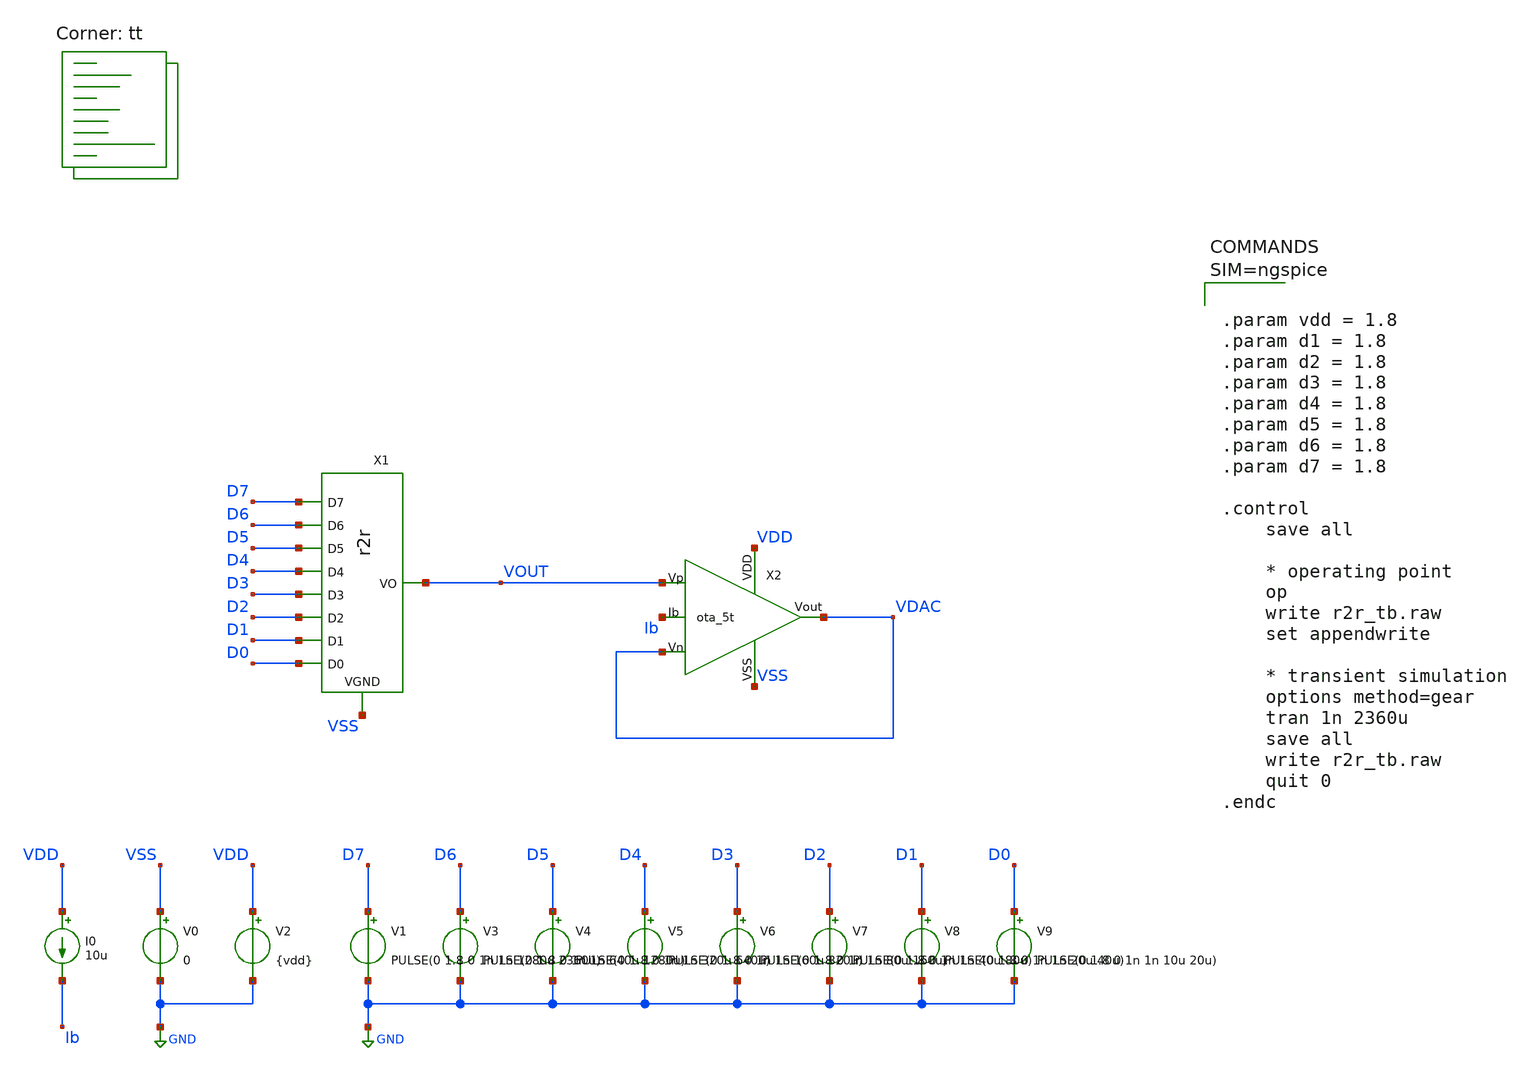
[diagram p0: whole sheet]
** sch_path: xschem/dac_tb.sch
**.subckt dac_tb
X1 D7 D6 D5 D4 D3 D2 D1 D0 VOUT VSS r2r
V0 VSS GND 0
V2 VDD GND {vdd}
V9 D0 GND PULSE(0 1.8 0 1n 1n 10u 20u)
V8 D1 GND PULSE(0 1.8 0 1n 1n 20u 40u)
V7 D2 GND PULSE(0 1.8 0 1n 1n 40u 80u)
V6 D3 GND PULSE(0 1.8 0 1n 1n 80u 160u)
V5 D4 GND PULSE(0 1.8 0 1n 1n 160u 320u)
V4 D5 GND PULSE(0 1.8 0 1n 1n 320u 640u)
V3 D6 GND PULSE(0 1.8 0 1n 1n 640u 1280u)
V1 D7 GND PULSE(0 1.8 0 1n 1n 1280u 2360u)
X2 Ib VDAC VOUT VDAC VDD VSS ota_5t
I0 VDD Ib 10u
**** begin user architecture code



.param vdd = 1.8
.param d1 = 1.8
.param d2 = 1.8
.param d3 = 1.8
.param d4 = 1.8
.param d5 = 1.8
.param d6 = 1.8
.param d7 = 1.8

.control
    save all

    * operating point
    op
    write r2r_tb.raw
    set appendwrite

    * transient simulation
    options method=gear
    tran 1n 2360u
    save all
    write r2r_tb.raw
    quit 0
.endc



.lib $::SKYWATER_MODELS/sky130.lib.spice tt
**** end user architecture code
**.ends

* expanding   symbol:  analog/projects/sky130/r2r-dac/xschem/r2r.sym # of pins=10
** sym_path: xschem/r2r.sym
** sch_path: xschem/r2r.sch
.subckt r2r D7 D6 D5 D4 D3 D2 D1 D0 VO VGND
*.ipin D0
*.ipin D1
*.ipin D2
*.ipin D3
*.ipin D4
*.ipin D5
*.ipin D6
*.ipin D7
*.opin VO
*.iopin VGND
XR8 net1 VGND VGND sky130_fd_pr__res_high_po_1p41 L=50 mult=1 m=1
XR1 net2 net1 VGND sky130_fd_pr__res_high_po_1p41 L=50 mult=1 m=1
XR2 net3 D0 VGND sky130_fd_pr__res_high_po_1p41 L=50 mult=1 m=1
XR3 net2 net3 VGND sky130_fd_pr__res_high_po_1p41 L=50 mult=1 m=1
XR4 net2 net5 VGND sky130_fd_pr__res_high_po_1p41 L=50 mult=1 m=1
XR5 net4 D1 VGND sky130_fd_pr__res_high_po_1p41 L=50 mult=1 m=1
XR6 net5 net4 VGND sky130_fd_pr__res_high_po_1p41 L=50 mult=1 m=1
XR7 net5 net6 VGND sky130_fd_pr__res_high_po_1p41 L=50 mult=1 m=1
XR9 net7 D2 VGND sky130_fd_pr__res_high_po_1p41 L=50 mult=1 m=1
XR10 net6 net7 VGND sky130_fd_pr__res_high_po_1p41 L=50 mult=1 m=1
XR11 net6 net8 VGND sky130_fd_pr__res_high_po_1p41 L=50 mult=1 m=1
XR12 net9 D3 VGND sky130_fd_pr__res_high_po_1p41 L=50 mult=1 m=1
XR13 net8 net9 VGND sky130_fd_pr__res_high_po_1p41 L=50 mult=1 m=1
XR14 net8 net10 VGND sky130_fd_pr__res_high_po_1p41 L=50 mult=1 m=1
XR15 net11 D4 VGND sky130_fd_pr__res_high_po_1p41 L=50 mult=1 m=1
XR16 net10 net11 VGND sky130_fd_pr__res_high_po_1p41 L=50 mult=1 m=1
XR17 net10 net12 VGND sky130_fd_pr__res_high_po_1p41 L=50 mult=1 m=1
XR18 net13 D5 VGND sky130_fd_pr__res_high_po_1p41 L=50 mult=1 m=1
XR19 net12 net13 VGND sky130_fd_pr__res_high_po_1p41 L=50 mult=1 m=1
XR20 net12 net14 VGND sky130_fd_pr__res_high_po_1p41 L=50 mult=1 m=1
XR21 net15 D6 VGND sky130_fd_pr__res_high_po_1p41 L=50 mult=1 m=1
XR22 net14 net15 VGND sky130_fd_pr__res_high_po_1p41 L=50 mult=1 m=1
XR23 net14 VO VGND sky130_fd_pr__res_high_po_1p41 L=50 mult=1 m=1
XR24 net16 D7 VGND sky130_fd_pr__res_high_po_1p41 L=50 mult=1 m=1
XR25 VO net16 VGND sky130_fd_pr__res_high_po_1p41 L=50 mult=1 m=1
.ends


* expanding   symbol:  analog/projects/sky130/r2r-dac/xschem/ota_5t.sym # of pins=6
** sym_path: xschem/ota_5t.sym
** sch_path: xschem/ota_5t.sch
.subckt ota_5t Ib Vn Vp Vout VDD VSS
*.iopin VDD
*.iopin VSS
*.opin Vout
*.ipin Vp
*.ipin Vn
*.ipin Ib
XM3 net2 Vp net1 VSS sky130_fd_pr__nfet_01v8 L=0.5 W=3 nf=1 ad='int((1 + 1)/2) * 3 / 1 * 0.29' as='int((1 + 2)/2) * 3 / 1 * 0.29'
+ pd='2*int((1 + 1)/2) * (3 / 1 + 0.29)' ps='2*int((1 + 2)/2) * (3 / 1 + 0.29)' nrd='0.29 / 3 ' nrs='0.29 / 3 '
+ sa=0 sb=0 sd=0 mult=1 m=1
XM1 net2 net2 VDD VDD sky130_fd_pr__pfet_01v8 L=1 W=4.5 nf=1 ad='int((nf+1)/2) * W/nf * 0.29' as='int((nf+2)/2) * W/nf * 0.29'
+ pd='2*int((nf+1)/2) * (W/nf + 0.29)' ps='2*int((nf+2)/2) * (W/nf + 0.29)' nrd='0.29 / W' nrs='0.29 / W'
+ sa=0 sb=0 sd=0 mult=1 m=1
XM2 Vout net2 VDD VDD sky130_fd_pr__pfet_01v8 L=1 W=4.5 nf=1 ad='int((nf+1)/2) * W/nf * 0.29' as='int((nf+2)/2) * W/nf * 0.29'
+ pd='2*int((nf+1)/2) * (W/nf + 0.29)' ps='2*int((nf+2)/2) * (W/nf + 0.29)' nrd='0.29 / W' nrs='0.29 / W'
+ sa=0 sb=0 sd=0 mult=1 m=1
XM4 Vout Vn net1 VSS sky130_fd_pr__nfet_01v8 L=0.5 W=3 nf=1 ad='int((1 + 1)/2) * 3 / 1 * 0.29' as='int((1 + 2)/2) * 3 / 1 * 0.29'
+ pd='2*int((1 + 1)/2) * (3 / 1 + 0.29)' ps='2*int((1 + 2)/2) * (3 / 1 + 0.29)' nrd='0.29 / 3 ' nrs='0.29 / 3 '
+ sa=0 sb=0 sd=0 mult=1 m=1
XM5 net1 Ib VSS VSS sky130_fd_pr__nfet_01v8 L=1 W=4 nf=1 ad='int((1 + 1)/2) * 4 / 1 * 0.29' as='int((1 + 2)/2) * 4 / 1 * 0.29'
+ pd='2*int((1 + 1)/2) * (4 / 1 + 0.29)' ps='2*int((1 + 2)/2) * (4 / 1 + 0.29)' nrd='0.29 / 4 ' nrs='0.29 / 4 '
+ sa=0 sb=0 sd=0 mult=1 m=1
XM6 Ib Ib VSS VSS sky130_fd_pr__nfet_01v8 L=1 W=4 nf=1 ad='int((1 + 1)/2) * 4 / 1 * 0.29' as='int((1 + 2)/2) * 4 / 1 * 0.29'
+ pd='2*int((1 + 1)/2) * (4 / 1 + 0.29)' ps='2*int((1 + 2)/2) * (4 / 1 + 0.29)' nrd='0.29 / 4 ' nrs='0.29 / 4 '
+ sa=0 sb=0 sd=0 mult=1 m=1
.ends

.GLOBAL GND
.end
